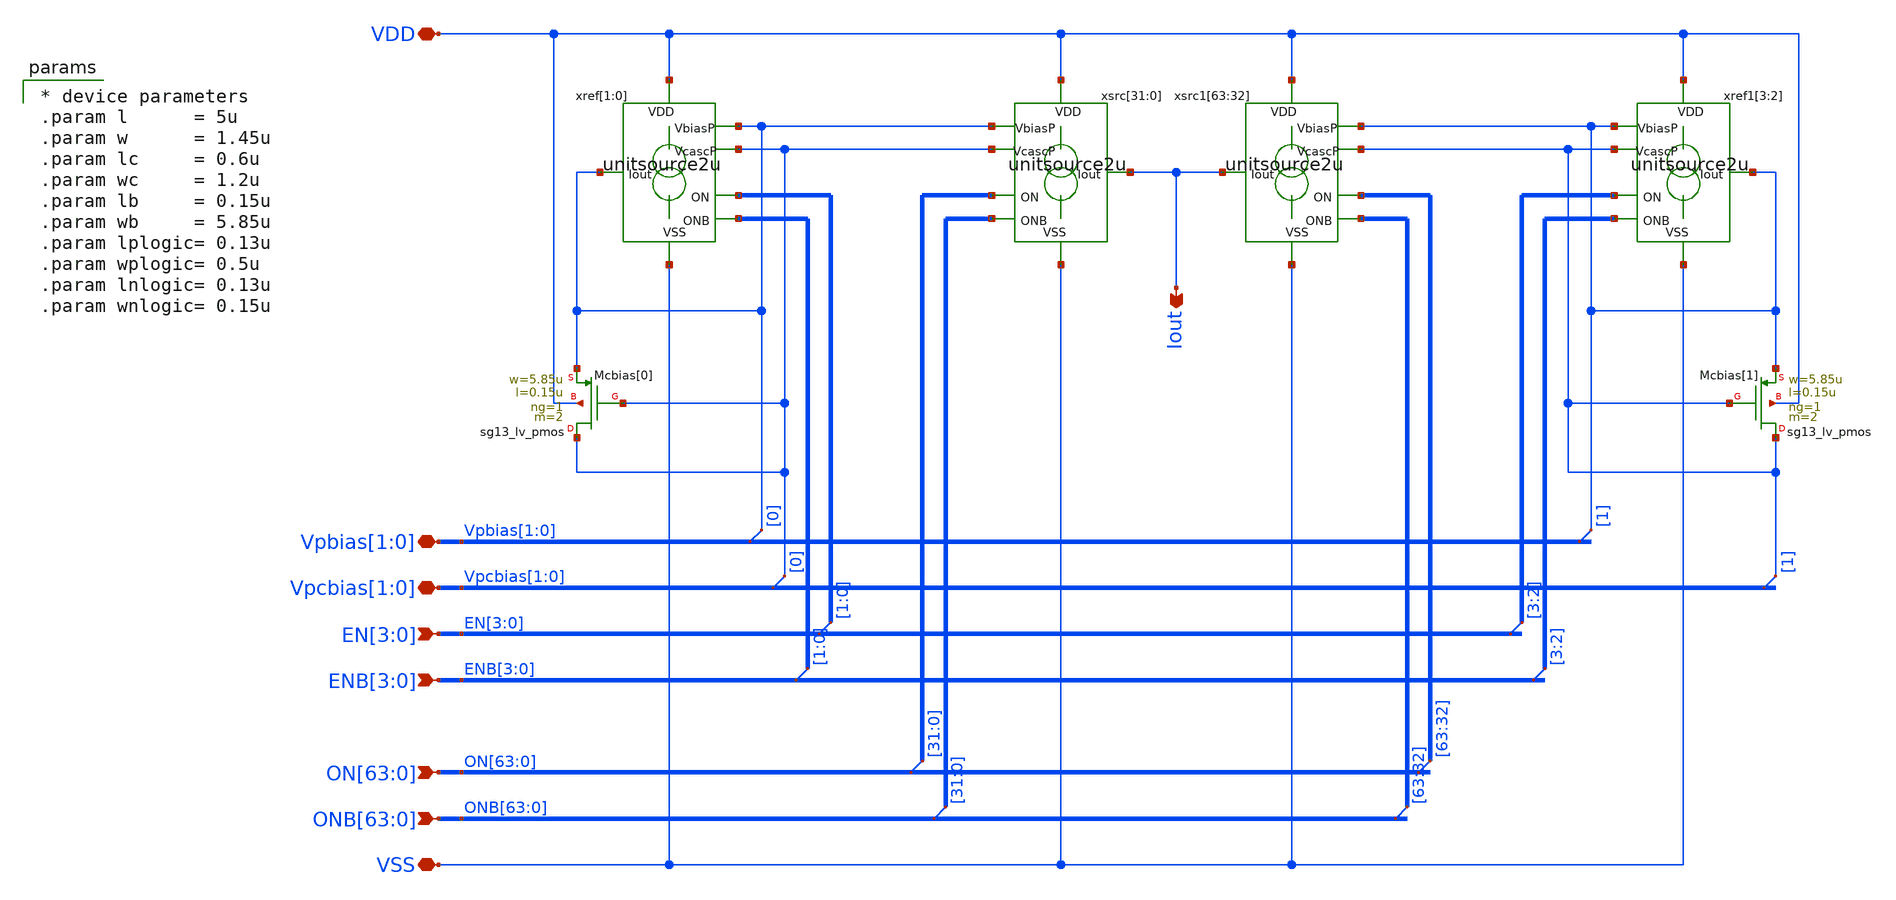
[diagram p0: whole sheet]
** sch_path: xschem/dac64module.sch
**.subckt dac64module Iout
*+ ON[63],ON[62],ON[61],ON[60],ON[59],ON[58],ON[57],ON[56],ON[55],ON[54],ON[53],ON[52],ON[51],ON[50],ON[49],ON[48],ON[47],ON[46],ON[45],ON[44],ON[43],ON[42],ON[41],ON[40],ON[39],ON[38],ON[37],ON[36],ON[35],ON[34],ON[33],ON[32],ON[31],ON[30],ON[29],ON[28],ON[27],ON[26],ON[25],ON[24],ON[23],ON[22],ON[21],ON[20],ON[19],ON[18],ON[17],ON[16],ON[15],ON[14],ON[13],ON[12],ON[11],ON[10],ON[9],ON[8],ON[7],ON[6],ON[5],ON[4],ON[3],ON[2],ON[1],ON[0]
*+ ONB[63],ONB[62],ONB[61],ONB[60],ONB[59],ONB[58],ONB[57],ONB[56],ONB[55],ONB[54],ONB[53],ONB[52],ONB[51],ONB[50],ONB[49],ONB[48],ONB[47],ONB[46],ONB[45],ONB[44],ONB[43],ONB[42],ONB[41],ONB[40],ONB[39],ONB[38],ONB[37],ONB[36],ONB[35],ONB[34],ONB[33],ONB[32],ONB[31],ONB[30],ONB[29],ONB[28],ONB[27],ONB[26],ONB[25],ONB[24],ONB[23],ONB[22],ONB[21],ONB[20],ONB[19],ONB[18],ONB[17],ONB[16],ONB[15],ONB[14],ONB[13],ONB[12],ONB[11],ONB[10],ONB[9],ONB[8],ONB[7],ONB[6],ONB[5],ONB[4],ONB[3],ONB[2],ONB[1],ONB[0] VSS VDD Vpcbias[1],Vpcbias[0] EN[3],EN[2],EN[1],EN[0] ENB[3],ENB[2],ENB[1],ENB[0]
*+ Vpbias[1],Vpbias[0]
*.opin Iout
*.ipin
*+ ON[63],ON[62],ON[61],ON[60],ON[59],ON[58],ON[57],ON[56],ON[55],ON[54],ON[53],ON[52],ON[51],ON[50],ON[49],ON[48],ON[47],ON[46],ON[45],ON[44],ON[43],ON[42],ON[41],ON[40],ON[39],ON[38],ON[37],ON[36],ON[35],ON[34],ON[33],ON[32],ON[31],ON[30],ON[29],ON[28],ON[27],ON[26],ON[25],ON[24],ON[23],ON[22],ON[21],ON[20],ON[19],ON[18],ON[17],ON[16],ON[15],ON[14],ON[13],ON[12],ON[11],ON[10],ON[9],ON[8],ON[7],ON[6],ON[5],ON[4],ON[3],ON[2],ON[1],ON[0]
*.ipin
*+ ONB[63],ONB[62],ONB[61],ONB[60],ONB[59],ONB[58],ONB[57],ONB[56],ONB[55],ONB[54],ONB[53],ONB[52],ONB[51],ONB[50],ONB[49],ONB[48],ONB[47],ONB[46],ONB[45],ONB[44],ONB[43],ONB[42],ONB[41],ONB[40],ONB[39],ONB[38],ONB[37],ONB[36],ONB[35],ONB[34],ONB[33],ONB[32],ONB[31],ONB[30],ONB[29],ONB[28],ONB[27],ONB[26],ONB[25],ONB[24],ONB[23],ONB[22],ONB[21],ONB[20],ONB[19],ONB[18],ONB[17],ONB[16],ONB[15],ONB[14],ONB[13],ONB[12],ONB[11],ONB[10],ONB[9],ONB[8],ONB[7],ONB[6],ONB[5],ONB[4],ONB[3],ONB[2],ONB[1],ONB[0]
*.iopin VSS
*.iopin VDD
*.iopin Vpcbias[1],Vpcbias[0]
*.ipin EN[3],EN[2],EN[1],EN[0]
*.ipin ENB[3],ENB[2],ENB[1],ENB[0]
*.iopin Vpbias[1],Vpbias[0]
XMcbias[0] Vpcbias[0] Vpcbias[0] Vpbias[0] VDD sg13_lv_pmos w=5.85u l=0.15u ng=1 m=2 mm_ok=1
xref[1] VDD Vpbias[0] EN[1] ENB[1] Vpbias[0] Vpcbias[0] VSS unitsource2u
xref[0] VDD Vpbias[0] EN[0] ENB[0] Vpbias[0] Vpcbias[0] VSS unitsource2u
xsrc[31] VDD Vpbias[0] ON[31] ONB[31] Iout Vpcbias[0] VSS unitsource2u
xsrc[30] VDD Vpbias[0] ON[30] ONB[30] Iout Vpcbias[0] VSS unitsource2u
xsrc[29] VDD Vpbias[0] ON[29] ONB[29] Iout Vpcbias[0] VSS unitsource2u
xsrc[28] VDD Vpbias[0] ON[28] ONB[28] Iout Vpcbias[0] VSS unitsource2u
xsrc[27] VDD Vpbias[0] ON[27] ONB[27] Iout Vpcbias[0] VSS unitsource2u
xsrc[26] VDD Vpbias[0] ON[26] ONB[26] Iout Vpcbias[0] VSS unitsource2u
xsrc[25] VDD Vpbias[0] ON[25] ONB[25] Iout Vpcbias[0] VSS unitsource2u
xsrc[24] VDD Vpbias[0] ON[24] ONB[24] Iout Vpcbias[0] VSS unitsource2u
xsrc[23] VDD Vpbias[0] ON[23] ONB[23] Iout Vpcbias[0] VSS unitsource2u
xsrc[22] VDD Vpbias[0] ON[22] ONB[22] Iout Vpcbias[0] VSS unitsource2u
xsrc[21] VDD Vpbias[0] ON[21] ONB[21] Iout Vpcbias[0] VSS unitsource2u
xsrc[20] VDD Vpbias[0] ON[20] ONB[20] Iout Vpcbias[0] VSS unitsource2u
xsrc[19] VDD Vpbias[0] ON[19] ONB[19] Iout Vpcbias[0] VSS unitsource2u
xsrc[18] VDD Vpbias[0] ON[18] ONB[18] Iout Vpcbias[0] VSS unitsource2u
xsrc[17] VDD Vpbias[0] ON[17] ONB[17] Iout Vpcbias[0] VSS unitsource2u
xsrc[16] VDD Vpbias[0] ON[16] ONB[16] Iout Vpcbias[0] VSS unitsource2u
xsrc[15] VDD Vpbias[0] ON[15] ONB[15] Iout Vpcbias[0] VSS unitsource2u
xsrc[14] VDD Vpbias[0] ON[14] ONB[14] Iout Vpcbias[0] VSS unitsource2u
xsrc[13] VDD Vpbias[0] ON[13] ONB[13] Iout Vpcbias[0] VSS unitsource2u
xsrc[12] VDD Vpbias[0] ON[12] ONB[12] Iout Vpcbias[0] VSS unitsource2u
xsrc[11] VDD Vpbias[0] ON[11] ONB[11] Iout Vpcbias[0] VSS unitsource2u
xsrc[10] VDD Vpbias[0] ON[10] ONB[10] Iout Vpcbias[0] VSS unitsource2u
xsrc[9] VDD Vpbias[0] ON[9] ONB[9] Iout Vpcbias[0] VSS unitsource2u
xsrc[8] VDD Vpbias[0] ON[8] ONB[8] Iout Vpcbias[0] VSS unitsource2u
xsrc[7] VDD Vpbias[0] ON[7] ONB[7] Iout Vpcbias[0] VSS unitsource2u
xsrc[6] VDD Vpbias[0] ON[6] ONB[6] Iout Vpcbias[0] VSS unitsource2u
xsrc[5] VDD Vpbias[0] ON[5] ONB[5] Iout Vpcbias[0] VSS unitsource2u
xsrc[4] VDD Vpbias[0] ON[4] ONB[4] Iout Vpcbias[0] VSS unitsource2u
xsrc[3] VDD Vpbias[0] ON[3] ONB[3] Iout Vpcbias[0] VSS unitsource2u
xsrc[2] VDD Vpbias[0] ON[2] ONB[2] Iout Vpcbias[0] VSS unitsource2u
xsrc[1] VDD Vpbias[0] ON[1] ONB[1] Iout Vpcbias[0] VSS unitsource2u
xsrc[0] VDD Vpbias[0] ON[0] ONB[0] Iout Vpcbias[0] VSS unitsource2u
XMcbias[1] Vpcbias[1] Vpcbias[1] Vpbias[1] VDD sg13_lv_pmos w=5.85u l=0.15u ng=1 m=2 mm_ok=1
xref1[3] VDD Vpbias[1] EN[3] ENB[3] Vpbias[1] Vpcbias[1] VSS unitsource2u
xref1[2] VDD Vpbias[1] EN[2] ENB[2] Vpbias[1] Vpcbias[1] VSS unitsource2u
xsrc1[63] VDD Vpbias[1] ON[63] ONB[63] Iout Vpcbias[1] VSS unitsource2u
xsrc1[62] VDD Vpbias[1] ON[62] ONB[62] Iout Vpcbias[1] VSS unitsource2u
xsrc1[61] VDD Vpbias[1] ON[61] ONB[61] Iout Vpcbias[1] VSS unitsource2u
xsrc1[60] VDD Vpbias[1] ON[60] ONB[60] Iout Vpcbias[1] VSS unitsource2u
xsrc1[59] VDD Vpbias[1] ON[59] ONB[59] Iout Vpcbias[1] VSS unitsource2u
xsrc1[58] VDD Vpbias[1] ON[58] ONB[58] Iout Vpcbias[1] VSS unitsource2u
xsrc1[57] VDD Vpbias[1] ON[57] ONB[57] Iout Vpcbias[1] VSS unitsource2u
xsrc1[56] VDD Vpbias[1] ON[56] ONB[56] Iout Vpcbias[1] VSS unitsource2u
xsrc1[55] VDD Vpbias[1] ON[55] ONB[55] Iout Vpcbias[1] VSS unitsource2u
xsrc1[54] VDD Vpbias[1] ON[54] ONB[54] Iout Vpcbias[1] VSS unitsource2u
xsrc1[53] VDD Vpbias[1] ON[53] ONB[53] Iout Vpcbias[1] VSS unitsource2u
xsrc1[52] VDD Vpbias[1] ON[52] ONB[52] Iout Vpcbias[1] VSS unitsource2u
xsrc1[51] VDD Vpbias[1] ON[51] ONB[51] Iout Vpcbias[1] VSS unitsource2u
xsrc1[50] VDD Vpbias[1] ON[50] ONB[50] Iout Vpcbias[1] VSS unitsource2u
xsrc1[49] VDD Vpbias[1] ON[49] ONB[49] Iout Vpcbias[1] VSS unitsource2u
xsrc1[48] VDD Vpbias[1] ON[48] ONB[48] Iout Vpcbias[1] VSS unitsource2u
xsrc1[47] VDD Vpbias[1] ON[47] ONB[47] Iout Vpcbias[1] VSS unitsource2u
xsrc1[46] VDD Vpbias[1] ON[46] ONB[46] Iout Vpcbias[1] VSS unitsource2u
xsrc1[45] VDD Vpbias[1] ON[45] ONB[45] Iout Vpcbias[1] VSS unitsource2u
xsrc1[44] VDD Vpbias[1] ON[44] ONB[44] Iout Vpcbias[1] VSS unitsource2u
xsrc1[43] VDD Vpbias[1] ON[43] ONB[43] Iout Vpcbias[1] VSS unitsource2u
xsrc1[42] VDD Vpbias[1] ON[42] ONB[42] Iout Vpcbias[1] VSS unitsource2u
xsrc1[41] VDD Vpbias[1] ON[41] ONB[41] Iout Vpcbias[1] VSS unitsource2u
xsrc1[40] VDD Vpbias[1] ON[40] ONB[40] Iout Vpcbias[1] VSS unitsource2u
xsrc1[39] VDD Vpbias[1] ON[39] ONB[39] Iout Vpcbias[1] VSS unitsource2u
xsrc1[38] VDD Vpbias[1] ON[38] ONB[38] Iout Vpcbias[1] VSS unitsource2u
xsrc1[37] VDD Vpbias[1] ON[37] ONB[37] Iout Vpcbias[1] VSS unitsource2u
xsrc1[36] VDD Vpbias[1] ON[36] ONB[36] Iout Vpcbias[1] VSS unitsource2u
xsrc1[35] VDD Vpbias[1] ON[35] ONB[35] Iout Vpcbias[1] VSS unitsource2u
xsrc1[34] VDD Vpbias[1] ON[34] ONB[34] Iout Vpcbias[1] VSS unitsource2u
xsrc1[33] VDD Vpbias[1] ON[33] ONB[33] Iout Vpcbias[1] VSS unitsource2u
xsrc1[32] VDD Vpbias[1] ON[32] ONB[32] Iout Vpcbias[1] VSS unitsource2u
* tap: EN[3:0] --> EN[1:0]
* tap: ENB[3:0] --> ENB[1:0]
* tap: ENB[3:0] --> ENB[3:2]
* tap: EN[3:0] --> EN[3:2]
* tap: ON[63:0] --> ON[31:0]
* tap: ONB[63:0] --> ONB[31:0]
* tap: ON[63:0] --> ON[63:32]
* tap: ONB[63:0] --> ONB[63:32]
* tap: Vpbias[1:0] --> Vpbias[0]
* tap: Vpcbias[1:0] --> Vpcbias[0]
* tap: Vpbias[1:0] --> Vpbias[1]
* tap: Vpcbias[1:0] --> Vpcbias[1]
**** begin user architecture code

* device parameters
.param l      = 5u
.param w      = 1.45u
.param lc     = 0.6u
.param wc     = 1.2u
.param lb     = 0.15u
.param wb     = 5.85u
.param lplogic= 0.13u
.param wplogic= 0.5u
.param lnlogic= 0.13u
.param wnlogic= 0.15u


**** end user architecture code
**.ends

* expanding   symbol:  unitsource2u.sym # of pins=7
** sym_path: xschem/unitsource2u.sym
** sch_path: xschem/unitsource2u.sch
.subckt unitsource2u VDD VbiasP ON ONB Iout VcascP VSS
*.iopin VSS
*.iopin VDD
*.iopin VbiasP
*.iopin VcascP
*.ipin ON
*.ipin ONB
*.iopin Iout
xnonoverlap VDD VSS ON ONB on_n off_n nonoverlap
xsw VDD off_n Vcasc on_n VcascP cascodeswitch_pmos
xsrc VDD VbiasP Vcasc Iout pcsource2u
.ends


* expanding   symbol:  nonoverlap.sym # of pins=6
** sym_path: xschem/nonoverlap.sym
** sch_path: xschem/nonoverlap.sch
.subckt nonoverlap VDD VSS INP INN OUTN OUTP
*.iopin VSS
*.iopin VDD
*.ipin INP
*.ipin INN
*.opin OUTP
*.opin OUTN
XM1 OUTN INP VDD VDD sg13_lv_pmos w=0.3u l=0.13u ng=1 m=1 mm_ok=1
XM2 OUTP INN VDD VDD sg13_lv_pmos w=0.3u l=0.13u ng=1 m=1 mm_ok=1
XM3 OUTN OUTP VSS VSS sg13_lv_nmos w=0.15u l=0.52u ng=1 m=1 mm_ok=1
XM4 OUTP OUTN VSS VSS sg13_lv_nmos w=0.15u l=0.52u ng=1 m=1 mm_ok=1
.ends


* expanding   symbol:  cascodeswitch_pmos.sym # of pins=5
** sym_path: xschem/cascodeswitch_pmos.sym
** sch_path: xschem/cascodeswitch_pmos.sch
.subckt cascodeswitch_pmos VDD off_n Vcasc on_n Vbpcasc
*.ipin off_n
*.ipin Vbpcasc
*.opin Vcasc
*.ipin on_n
*.ipin VDD
XMpullup Vcasc off_n VDD VDD sg13_lv_pmos w=0.3u l=0.13u ng=1 m=1 mm_ok=1
XMbias Vbpcasc on_n Vcasc VDD sg13_lv_pmos w=0.3u l=0.13u ng=1 m=1 mm_ok=1
.ends


* expanding   symbol:  pcsource2u.sym # of pins=4
** sym_path: xschem/pcsource2u.sym
** sch_path: xschem/pcsource2u.sch
.subckt pcsource2u VDD VbiasP VcascodeP Iout
*.ipin VcascodeP
*.ipin VbiasP
*.opin Iout
*.ipin VDD
XMsrc drain net4 VDD net1 sg13_lv_pmos w=1.45u l=5u ng=1 m=1 mm_ok=1
XMcasc Iout net3 drain net2 sg13_lv_pmos w=1.2u l=0.6u ng=1 m=1 mm_ok=1
Vgsrc net4 VbiasP 0
.save i(vgsrc)
Vgcasc net3 VcascodeP 0
.save i(vgcasc)
Vbsrc VDD net1 0
.save i(vbsrc)
Vbcasc VDD net2 0
.save i(vbcasc)
.ends

.end
